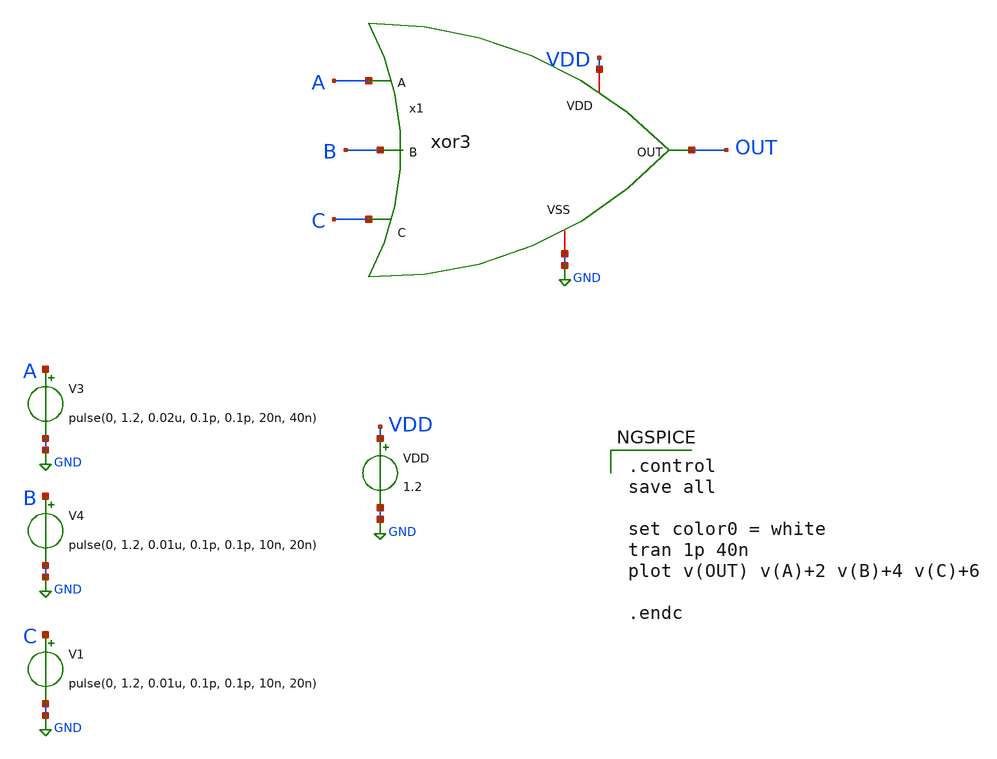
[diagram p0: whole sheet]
** sch_path: design/XOR3/xschem/xor3_tb.sch
**.subckt xor3_tb
VDD VDD GND 1.2
V3 A GND pulse(0, 1.2, 0.02u, 0.1p, 0.1p, 20n, 40n)
V4 B GND pulse(0, 1.2, 0.01u, 0.1p, 0.1p, 10n, 20n)
V1 C GND pulse(0, 1.2, 0.01u, 0.1p, 0.1p, 10n, 20n)
x1 VDD A OUT B C GND xor3
**** begin user architecture code

** opencircuitdesign pdks install
.lib $::SKYWATER_MODELS/sky130.lib.spice tt_mm



.control
save all

set color0 = white
tran 1p 40n
plot v(OUT) v(A)+2 v(B)+4 v(C)+6

.endc

**** end user architecture code
**.ends
.GLOBAL GND
.end
